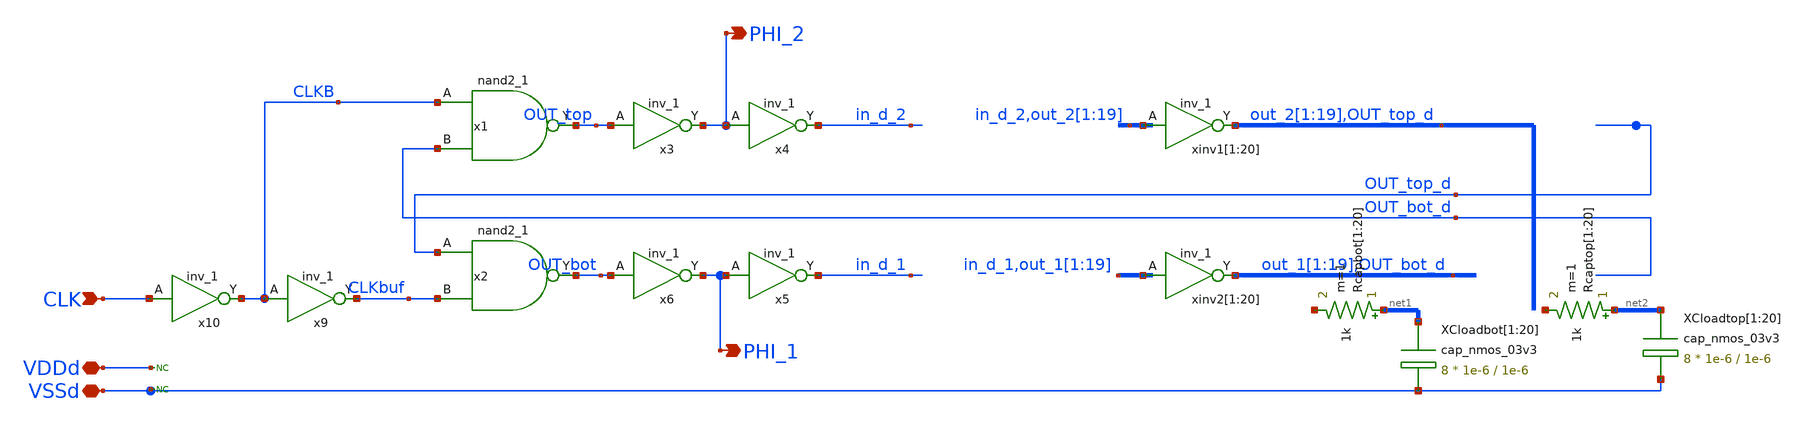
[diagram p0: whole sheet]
** sch_path: NO_ClkGen/NO_ClkGen_w_cap2.sch
**.subckt NO_ClkGen_w_cap2 CLK PHI_2 PHI_1 VDDd VSSd
*.ipin CLK
*.opin PHI_2
*.opin PHI_1
*.iopin VDDd
*.iopin VSSd
x1 CLKB OUT_bot_d VSSd VDDd VSSd VDDd OUT_top gf180mcu_fd_sc_mcu9t5v0__nand2_1
x2 OUT_top_d CLKbuf VSSd VDDd VSSd VDDd OUT_bot gf180mcu_fd_sc_mcu9t5v0__nand2_1
x3 OUT_top VSSd VDDd VSSd VDDd PHI_2 gf180mcu_fd_sc_mcu9t5v0__inv_1
x4 PHI_2 VSSd VDDd VSSd VDDd in_d_2 gf180mcu_fd_sc_mcu9t5v0__inv_1
x6 OUT_bot VSSd VDDd VSSd VDDd PHI_1 gf180mcu_fd_sc_mcu9t5v0__inv_1
x9 CLKB VSSd VDDd VSSd VDDd CLKbuf gf180mcu_fd_sc_mcu9t5v0__inv_1
x10 CLK VSSd VDDd VSSd VDDd CLKB gf180mcu_fd_sc_mcu9t5v0__inv_1
* noconn VDDd
* noconn VSSd
xinv1[1] in_d_2 VSSd VDDd VSSd VDDd out_2[1] gf180mcu_fd_sc_mcu9t5v0__inv_1
xinv1[2] out_2[1] VSSd VDDd VSSd VDDd out_2[2] gf180mcu_fd_sc_mcu9t5v0__inv_1
xinv1[3] out_2[2] VSSd VDDd VSSd VDDd out_2[3] gf180mcu_fd_sc_mcu9t5v0__inv_1
xinv1[4] out_2[3] VSSd VDDd VSSd VDDd out_2[4] gf180mcu_fd_sc_mcu9t5v0__inv_1
xinv1[5] out_2[4] VSSd VDDd VSSd VDDd out_2[5] gf180mcu_fd_sc_mcu9t5v0__inv_1
xinv1[6] out_2[5] VSSd VDDd VSSd VDDd out_2[6] gf180mcu_fd_sc_mcu9t5v0__inv_1
xinv1[7] out_2[6] VSSd VDDd VSSd VDDd out_2[7] gf180mcu_fd_sc_mcu9t5v0__inv_1
xinv1[8] out_2[7] VSSd VDDd VSSd VDDd out_2[8] gf180mcu_fd_sc_mcu9t5v0__inv_1
xinv1[9] out_2[8] VSSd VDDd VSSd VDDd out_2[9] gf180mcu_fd_sc_mcu9t5v0__inv_1
xinv1[10] out_2[9] VSSd VDDd VSSd VDDd out_2[10] gf180mcu_fd_sc_mcu9t5v0__inv_1
xinv1[11] out_2[10] VSSd VDDd VSSd VDDd out_2[11] gf180mcu_fd_sc_mcu9t5v0__inv_1
xinv1[12] out_2[11] VSSd VDDd VSSd VDDd out_2[12] gf180mcu_fd_sc_mcu9t5v0__inv_1
xinv1[13] out_2[12] VSSd VDDd VSSd VDDd out_2[13] gf180mcu_fd_sc_mcu9t5v0__inv_1
xinv1[14] out_2[13] VSSd VDDd VSSd VDDd out_2[14] gf180mcu_fd_sc_mcu9t5v0__inv_1
xinv1[15] out_2[14] VSSd VDDd VSSd VDDd out_2[15] gf180mcu_fd_sc_mcu9t5v0__inv_1
xinv1[16] out_2[15] VSSd VDDd VSSd VDDd out_2[16] gf180mcu_fd_sc_mcu9t5v0__inv_1
xinv1[17] out_2[16] VSSd VDDd VSSd VDDd out_2[17] gf180mcu_fd_sc_mcu9t5v0__inv_1
xinv1[18] out_2[17] VSSd VDDd VSSd VDDd out_2[18] gf180mcu_fd_sc_mcu9t5v0__inv_1
xinv1[19] out_2[18] VSSd VDDd VSSd VDDd out_2[19] gf180mcu_fd_sc_mcu9t5v0__inv_1
xinv1[20] out_2[19] VSSd VDDd VSSd VDDd OUT_top_d gf180mcu_fd_sc_mcu9t5v0__inv_1
x5 PHI_1 VSSd VDDd VSSd VDDd in_d_1 gf180mcu_fd_sc_mcu9t5v0__inv_1
xinv2[1] in_d_1 VSSd VDDd VSSd VDDd out_1[1] gf180mcu_fd_sc_mcu9t5v0__inv_1
xinv2[2] out_1[1] VSSd VDDd VSSd VDDd out_1[2] gf180mcu_fd_sc_mcu9t5v0__inv_1
xinv2[3] out_1[2] VSSd VDDd VSSd VDDd out_1[3] gf180mcu_fd_sc_mcu9t5v0__inv_1
xinv2[4] out_1[3] VSSd VDDd VSSd VDDd out_1[4] gf180mcu_fd_sc_mcu9t5v0__inv_1
xinv2[5] out_1[4] VSSd VDDd VSSd VDDd out_1[5] gf180mcu_fd_sc_mcu9t5v0__inv_1
xinv2[6] out_1[5] VSSd VDDd VSSd VDDd out_1[6] gf180mcu_fd_sc_mcu9t5v0__inv_1
xinv2[7] out_1[6] VSSd VDDd VSSd VDDd out_1[7] gf180mcu_fd_sc_mcu9t5v0__inv_1
xinv2[8] out_1[7] VSSd VDDd VSSd VDDd out_1[8] gf180mcu_fd_sc_mcu9t5v0__inv_1
xinv2[9] out_1[8] VSSd VDDd VSSd VDDd out_1[9] gf180mcu_fd_sc_mcu9t5v0__inv_1
xinv2[10] out_1[9] VSSd VDDd VSSd VDDd out_1[10] gf180mcu_fd_sc_mcu9t5v0__inv_1
xinv2[11] out_1[10] VSSd VDDd VSSd VDDd out_1[11] gf180mcu_fd_sc_mcu9t5v0__inv_1
xinv2[12] out_1[11] VSSd VDDd VSSd VDDd out_1[12] gf180mcu_fd_sc_mcu9t5v0__inv_1
xinv2[13] out_1[12] VSSd VDDd VSSd VDDd out_1[13] gf180mcu_fd_sc_mcu9t5v0__inv_1
xinv2[14] out_1[13] VSSd VDDd VSSd VDDd out_1[14] gf180mcu_fd_sc_mcu9t5v0__inv_1
xinv2[15] out_1[14] VSSd VDDd VSSd VDDd out_1[15] gf180mcu_fd_sc_mcu9t5v0__inv_1
xinv2[16] out_1[15] VSSd VDDd VSSd VDDd out_1[16] gf180mcu_fd_sc_mcu9t5v0__inv_1
xinv2[17] out_1[16] VSSd VDDd VSSd VDDd out_1[17] gf180mcu_fd_sc_mcu9t5v0__inv_1
xinv2[18] out_1[17] VSSd VDDd VSSd VDDd out_1[18] gf180mcu_fd_sc_mcu9t5v0__inv_1
xinv2[19] out_1[18] VSSd VDDd VSSd VDDd out_1[19] gf180mcu_fd_sc_mcu9t5v0__inv_1
xinv2[20] out_1[19] VSSd VDDd VSSd VDDd OUT_bot_d gf180mcu_fd_sc_mcu9t5v0__inv_1
XCloadbot[1] net1[19] VSSd cap_nmos_03v3 c_width=1e-6 c_length=1e-6 m=8
XCloadbot[2] net1[18] VSSd cap_nmos_03v3 c_width=1e-6 c_length=1e-6 m=8
XCloadbot[3] net1[17] VSSd cap_nmos_03v3 c_width=1e-6 c_length=1e-6 m=8
XCloadbot[4] net1[16] VSSd cap_nmos_03v3 c_width=1e-6 c_length=1e-6 m=8
XCloadbot[5] net1[15] VSSd cap_nmos_03v3 c_width=1e-6 c_length=1e-6 m=8
XCloadbot[6] net1[14] VSSd cap_nmos_03v3 c_width=1e-6 c_length=1e-6 m=8
XCloadbot[7] net1[13] VSSd cap_nmos_03v3 c_width=1e-6 c_length=1e-6 m=8
XCloadbot[8] net1[12] VSSd cap_nmos_03v3 c_width=1e-6 c_length=1e-6 m=8
XCloadbot[9] net1[11] VSSd cap_nmos_03v3 c_width=1e-6 c_length=1e-6 m=8
XCloadbot[10] net1[10] VSSd cap_nmos_03v3 c_width=1e-6 c_length=1e-6 m=8
XCloadbot[11] net1[9] VSSd cap_nmos_03v3 c_width=1e-6 c_length=1e-6 m=8
XCloadbot[12] net1[8] VSSd cap_nmos_03v3 c_width=1e-6 c_length=1e-6 m=8
XCloadbot[13] net1[7] VSSd cap_nmos_03v3 c_width=1e-6 c_length=1e-6 m=8
XCloadbot[14] net1[6] VSSd cap_nmos_03v3 c_width=1e-6 c_length=1e-6 m=8
XCloadbot[15] net1[5] VSSd cap_nmos_03v3 c_width=1e-6 c_length=1e-6 m=8
XCloadbot[16] net1[4] VSSd cap_nmos_03v3 c_width=1e-6 c_length=1e-6 m=8
XCloadbot[17] net1[3] VSSd cap_nmos_03v3 c_width=1e-6 c_length=1e-6 m=8
XCloadbot[18] net1[2] VSSd cap_nmos_03v3 c_width=1e-6 c_length=1e-6 m=8
XCloadbot[19] net1[1] VSSd cap_nmos_03v3 c_width=1e-6 c_length=1e-6 m=8
XCloadbot[20] net1[0] VSSd cap_nmos_03v3 c_width=1e-6 c_length=1e-6 m=8
XCloadtop[1] net2[19] VSSd cap_nmos_03v3 c_width=1e-6 c_length=1e-6 m=8
XCloadtop[2] net2[18] VSSd cap_nmos_03v3 c_width=1e-6 c_length=1e-6 m=8
XCloadtop[3] net2[17] VSSd cap_nmos_03v3 c_width=1e-6 c_length=1e-6 m=8
XCloadtop[4] net2[16] VSSd cap_nmos_03v3 c_width=1e-6 c_length=1e-6 m=8
XCloadtop[5] net2[15] VSSd cap_nmos_03v3 c_width=1e-6 c_length=1e-6 m=8
XCloadtop[6] net2[14] VSSd cap_nmos_03v3 c_width=1e-6 c_length=1e-6 m=8
XCloadtop[7] net2[13] VSSd cap_nmos_03v3 c_width=1e-6 c_length=1e-6 m=8
XCloadtop[8] net2[12] VSSd cap_nmos_03v3 c_width=1e-6 c_length=1e-6 m=8
XCloadtop[9] net2[11] VSSd cap_nmos_03v3 c_width=1e-6 c_length=1e-6 m=8
XCloadtop[10] net2[10] VSSd cap_nmos_03v3 c_width=1e-6 c_length=1e-6 m=8
XCloadtop[11] net2[9] VSSd cap_nmos_03v3 c_width=1e-6 c_length=1e-6 m=8
XCloadtop[12] net2[8] VSSd cap_nmos_03v3 c_width=1e-6 c_length=1e-6 m=8
XCloadtop[13] net2[7] VSSd cap_nmos_03v3 c_width=1e-6 c_length=1e-6 m=8
XCloadtop[14] net2[6] VSSd cap_nmos_03v3 c_width=1e-6 c_length=1e-6 m=8
XCloadtop[15] net2[5] VSSd cap_nmos_03v3 c_width=1e-6 c_length=1e-6 m=8
XCloadtop[16] net2[4] VSSd cap_nmos_03v3 c_width=1e-6 c_length=1e-6 m=8
XCloadtop[17] net2[3] VSSd cap_nmos_03v3 c_width=1e-6 c_length=1e-6 m=8
XCloadtop[18] net2[2] VSSd cap_nmos_03v3 c_width=1e-6 c_length=1e-6 m=8
XCloadtop[19] net2[1] VSSd cap_nmos_03v3 c_width=1e-6 c_length=1e-6 m=8
XCloadtop[20] net2[0] VSSd cap_nmos_03v3 c_width=1e-6 c_length=1e-6 m=8
Rcapbot[1] net1[19] net3[19] 1k m=1
Rcapbot[2] net1[18] net3[18] 1k m=1
Rcapbot[3] net1[17] net3[17] 1k m=1
Rcapbot[4] net1[16] net3[16] 1k m=1
Rcapbot[5] net1[15] net3[15] 1k m=1
Rcapbot[6] net1[14] net3[14] 1k m=1
Rcapbot[7] net1[13] net3[13] 1k m=1
Rcapbot[8] net1[12] net3[12] 1k m=1
Rcapbot[9] net1[11] net3[11] 1k m=1
Rcapbot[10] net1[10] net3[10] 1k m=1
Rcapbot[11] net1[9] net3[9] 1k m=1
Rcapbot[12] net1[8] net3[8] 1k m=1
Rcapbot[13] net1[7] net3[7] 1k m=1
Rcapbot[14] net1[6] net3[6] 1k m=1
Rcapbot[15] net1[5] net3[5] 1k m=1
Rcapbot[16] net1[4] net3[4] 1k m=1
Rcapbot[17] net1[3] net3[3] 1k m=1
Rcapbot[18] net1[2] net3[2] 1k m=1
Rcapbot[19] net1[1] net3[1] 1k m=1
Rcapbot[20] net1[0] net3[0] 1k m=1
Rcaptop[1] net2[19] net4[19] 1k m=1
Rcaptop[2] net2[18] net4[18] 1k m=1
Rcaptop[3] net2[17] net4[17] 1k m=1
Rcaptop[4] net2[16] net4[16] 1k m=1
Rcaptop[5] net2[15] net4[15] 1k m=1
Rcaptop[6] net2[14] net4[14] 1k m=1
Rcaptop[7] net2[13] net4[13] 1k m=1
Rcaptop[8] net2[12] net4[12] 1k m=1
Rcaptop[9] net2[11] net4[11] 1k m=1
Rcaptop[10] net2[10] net4[10] 1k m=1
Rcaptop[11] net2[9] net4[9] 1k m=1
Rcaptop[12] net2[8] net4[8] 1k m=1
Rcaptop[13] net2[7] net4[7] 1k m=1
Rcaptop[14] net2[6] net4[6] 1k m=1
Rcaptop[15] net2[5] net4[5] 1k m=1
Rcaptop[16] net2[4] net4[4] 1k m=1
Rcaptop[17] net2[3] net4[3] 1k m=1
Rcaptop[18] net2[2] net4[2] 1k m=1
Rcaptop[19] net2[1] net4[1] 1k m=1
Rcaptop[20] net2[0] net4[0] 1k m=1
**.ends
.end
